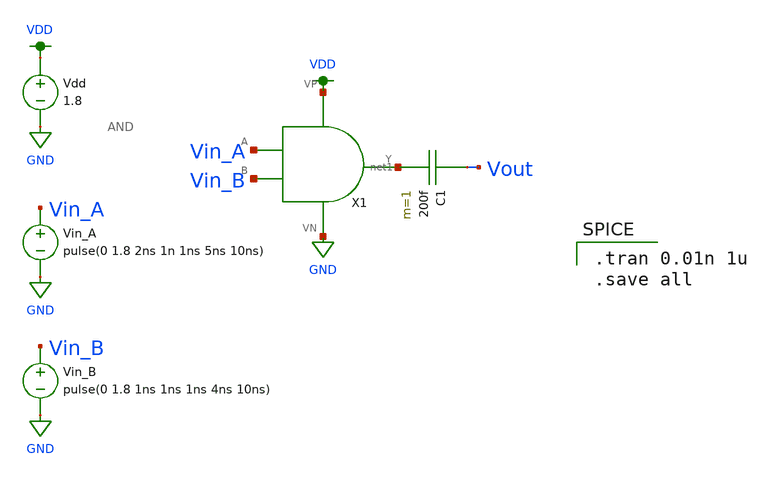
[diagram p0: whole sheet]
** sch_path: MP1/xschem/AND_sym_tran.sch
**.subckt AND_sym_tran
X1 Vin_A Vin_B net1 VDD GND AND
Vdd VDD GND 1.8
Vin_A Vin_A GND pulse(0 1.8 2ns 1n 1ns 5ns 10ns)
Vin_B Vin_B GND pulse(0 1.8 1ns 1ns 1ns 4ns 10ns)
C1 Vout net1 200f m=1
**** begin user architecture code

.option wnflag=1
.lib ~/skywater/skywater-pdk/libraries/sky130_fd_pr_ngspice/latest/models/sky130.lib.spice tt


.tran 0.01n 1u
.save all

**** end user architecture code
**.ends
.GLOBAL VDD
.GLOBAL GND
.end
